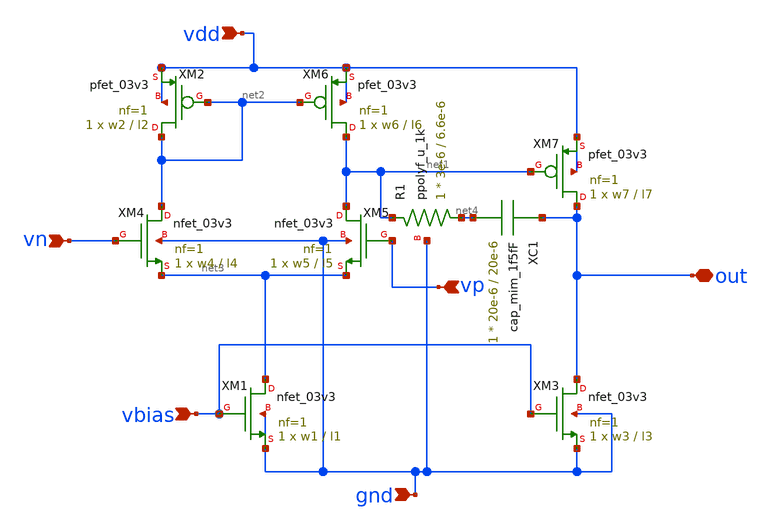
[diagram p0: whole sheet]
** sch_path: OpAmP/opamp_poly.sch
**.subckt opamp_poly gnd out vbias vp vn vdd
*.ipin gnd
*.iopin out
*.ipin vbias
*.ipin vp
*.ipin vn
*.ipin vdd
XM1 net3 vbias gnd gnd nfet_03v3 L=l1 W=w1 nf=1 ad='int((nf+1)/2) * W/nf * 0.18u' as='int((nf+2)/2) * W/nf * 0.18u'
+ pd='2*int((nf+1)/2) * (W/nf + 0.18u)' ps='2*int((nf+2)/2) * (W/nf + 0.18u)' nrd='0.18u / W' nrs='0.18u / W'
+ sa=0 sb=0 sd=0 m=1
XM2 net2 net2 vdd vdd pfet_03v3 L=l2 W=w2 nf=1 ad='int((nf+1)/2) * W/nf * 0.18u' as='int((nf+2)/2) * W/nf * 0.18u'
+ pd='2*int((nf+1)/2) * (W/nf + 0.18u)' ps='2*int((nf+2)/2) * (W/nf + 0.18u)' nrd='0.18u / W' nrs='0.18u / W'
+ sa=0 sb=0 sd=0 m=1
XM3 out vbias gnd gnd nfet_03v3 L=l3 W=w3 nf=1 ad='int((nf+1)/2) * W/nf * 0.18u' as='int((nf+2)/2) * W/nf * 0.18u'
+ pd='2*int((nf+1)/2) * (W/nf + 0.18u)' ps='2*int((nf+2)/2) * (W/nf + 0.18u)' nrd='0.18u / W' nrs='0.18u / W'
+ sa=0 sb=0 sd=0 m=1
XM4 net2 vn net3 gnd nfet_03v3 L=l4 W=w4 nf=1 ad='int((nf+1)/2) * W/nf * 0.18u' as='int((nf+2)/2) * W/nf * 0.18u'
+ pd='2*int((nf+1)/2) * (W/nf + 0.18u)' ps='2*int((nf+2)/2) * (W/nf + 0.18u)' nrd='0.18u / W' nrs='0.18u / W'
+ sa=0 sb=0 sd=0 m=1
XM5 net1 vp net3 gnd nfet_03v3 L=l5 W=w5 nf=1 ad='int((nf+1)/2) * W/nf * 0.18u' as='int((nf+2)/2) * W/nf * 0.18u'
+ pd='2*int((nf+1)/2) * (W/nf + 0.18u)' ps='2*int((nf+2)/2) * (W/nf + 0.18u)' nrd='0.18u / W' nrs='0.18u / W'
+ sa=0 sb=0 sd=0 m=1
XM6 net1 net2 vdd vdd pfet_03v3 L=l6 W=w6 nf=1 ad='int((nf+1)/2) * W/nf * 0.18u' as='int((nf+2)/2) * W/nf * 0.18u'
+ pd='2*int((nf+1)/2) * (W/nf + 0.18u)' ps='2*int((nf+2)/2) * (W/nf + 0.18u)' nrd='0.18u / W' nrs='0.18u / W'
+ sa=0 sb=0 sd=0 m=1
XM7 out net1 vdd vdd pfet_03v3 L=l7 W=w7 nf=1 ad='int((nf+1)/2) * W/nf * 0.18u' as='int((nf+2)/2) * W/nf * 0.18u'
+ pd='2*int((nf+1)/2) * (W/nf + 0.18u)' ps='2*int((nf+2)/2) * (W/nf + 0.18u)' nrd='0.18u / W' nrs='0.18u / W'
+ sa=0 sb=0 sd=0 m=1
XR1 net4 net1 gnd ppolyf_u_1k r_width=3e-6 r_length=6.6e-6 m=1
XC1 out net4 cap_mim_1f5fF c_width=20e-6 c_length=20e-6 m=1
**.ends
.end
